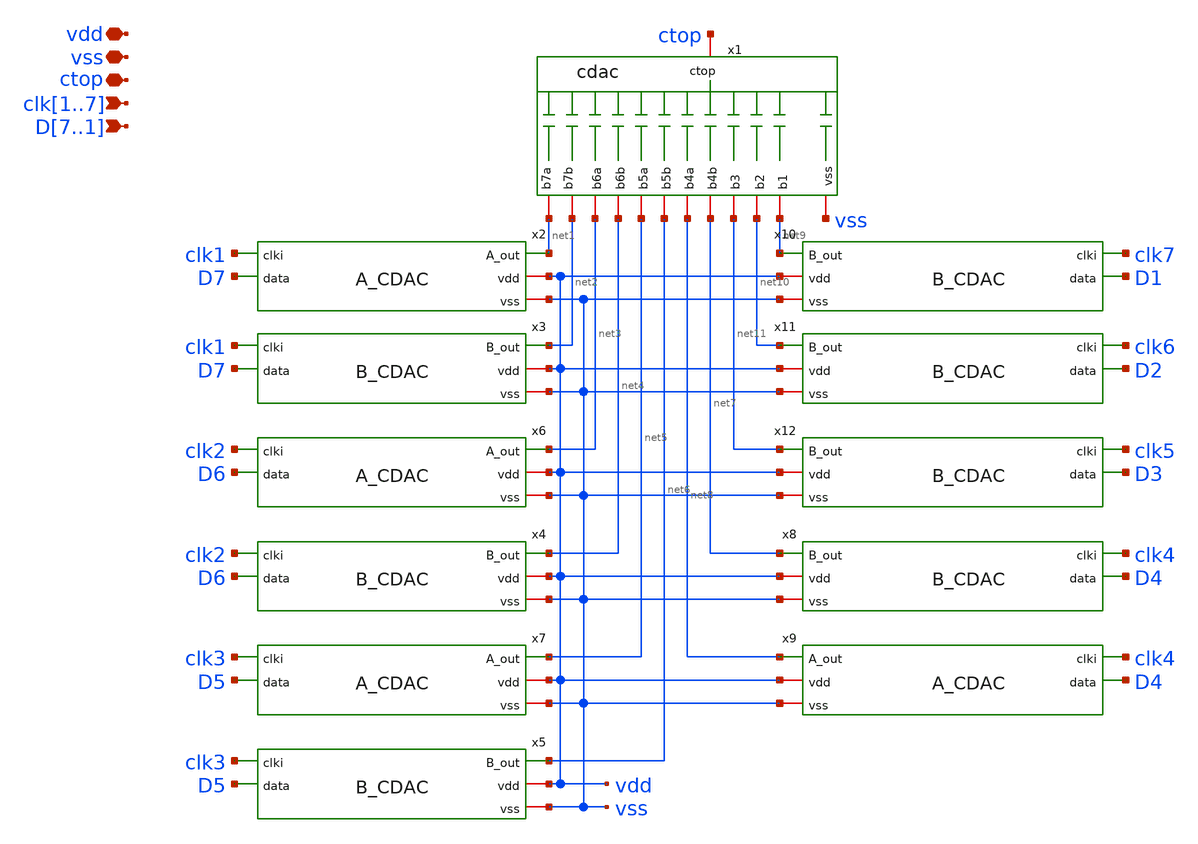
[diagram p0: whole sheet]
** sch_path: xschem/sar-adc/CDACnDriver.sch
**.subckt CDACnDriver D7,D6,D5,D4,D3,D2,D1 vdd vss clk1,clk2,clk3,clk4,clk5,clk6,clk7 ctop
*.ipin D7,D6,D5,D4,D3,D2,D1
*.iopin vdd
*.iopin vss
*.ipin clk1,clk2,clk3,clk4,clk5,clk6,clk7
*.iopin ctop
x1 ctop net9 net10 net1 net8 net6 net4 net11 vss net7 net5 net3 net2 cdac
x2 clk1 D7 net1 vdd vss A_CDAC
x3 clk1 D7 net2 vdd vss B_CDAC
x4 clk2 D6 net4 vdd vss B_CDAC
x5 clk3 D5 net6 vdd vss B_CDAC
x6 clk2 D6 net3 vdd vss A_CDAC
x7 clk3 D5 net5 vdd vss A_CDAC
x8 clk4 D4 net7 vdd vss B_CDAC
x9 clk4 D4 net8 vdd vss A_CDAC
x10 clk7 D1 net9 vdd vss B_CDAC
x11 clk6 D2 net10 vdd vss B_CDAC
x12 clk5 D3 net11 vdd vss B_CDAC
**.ends

* expanding   symbol:  cdac.sym # of pins=13
** sym_path: xschem/sar-adc/cdac.sym
** sch_path: xschem/sar-adc/cdac.sch
.subckt cdac ctop b1 b2 b7a b4a b5b b6b b3 vss b4b b5a b6a b7b
*.iopin ctop
*.iopin b1
*.iopin b2
*.iopin b7a
*.iopin b4a
*.iopin b5a
*.iopin b6a
*.iopin b3
*.iopin b5b
*.iopin b4b
*.iopin b6b
*.iopin b7b
*.iopin vss
XC6b ctop b6b sky130_fd_pr__cap_mim_m3_1 W=2 L=2 MF=16 m=16
XC1 ctop b1 sky130_fd_pr__cap_mim_m3_1 W=2 L=2 MF=1 m=1
XC2 ctop b2 sky130_fd_pr__cap_mim_m3_1 W=2 L=2 MF=2 m=2
XC3b ctop b3 sky130_fd_pr__cap_mim_m3_1 W=2 L=2 MF=4 m=4
XC4b ctop b4b sky130_fd_pr__cap_mim_m3_1 W=2 L=2 MF=4 m=4
XC5b ctop b5b sky130_fd_pr__cap_mim_m3_1 W=2 L=2 MF=8 m=8
XC7b ctop b7b sky130_fd_pr__cap_mim_m3_1 W=2 L=2 MF=32 m=32
XCdummy ctop vss sky130_fd_pr__cap_mim_m3_1 W=2 L=2 MF=1 m=1
XC7a ctop b7a sky130_fd_pr__cap_mim_m3_1 W=2 L=2 MF=32 m=32
XC5a ctop b5a sky130_fd_pr__cap_mim_m3_1 W=2 L=2 MF=8 m=8
XC4a ctop b4a sky130_fd_pr__cap_mim_m3_1 W=2 L=2 MF=4 m=4
XC6a ctop b6a sky130_fd_pr__cap_mim_m3_1 W=2 L=2 MF=16 m=16
XCdummy1 ctop ctop sky130_fd_pr__cap_mim_m3_1 W=2 L=2 MF=68 m=68
.ends


* expanding   symbol:  A_CDAC.sym # of pins=5
** sym_path: xschem/sar-adc/A_CDAC.sym
** sch_path: xschem/sar-adc/A_CDAC.sch
.subckt A_CDAC clki data A_out vdd vss
*.ipin data
*.opin A_out
*.iopin vdd
*.iopin vss
*.ipin clki
x1 data clki vss vss vdd vdd A_out sky130_fd_sc_hd__and2b_4
.ends


* expanding   symbol:  B_CDAC.sym # of pins=5
** sym_path: xschem/sar-adc/B_CDAC.sym
** sch_path: xschem/sar-adc/B_CDAC.sch
.subckt B_CDAC clki data B_out vdd vss
*.ipin data
*.opin B_out
*.iopin vdd
*.iopin vss
*.ipin clki
x1 clki data vss vss vdd vdd B_out sky130_fd_sc_hd__nand2_4
.ends

.end
